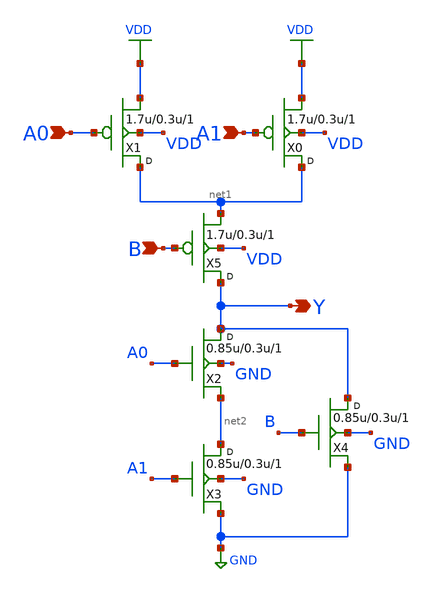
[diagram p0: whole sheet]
** sch_path: openfasoc/common/platforms/gf180mcuosu9Taoi211/gf180mcu_osu_sc_aoi21_1.sch
**.subckt gf180mcu_osu_sc_aoi21_1 A0 A1 Y B
*.ipin A0
*.ipin A1
*.opin Y
*.ipin B
X1 net1 A0 VDD VDD pmos_3p3 w=1.7u l=0.3u m=1
X0 net1 A1 VDD VDD pmos_3p3 w=1.7u l=0.3u m=1
X2 Y A0 net2 GND nmos_3p3 w=0.85u l=0.3u m=1
X3 net2 A1 GND GND nmos_3p3 w=0.85u l=0.3u m=1
X4 Y B GND GND nmos_3p3 w=0.85u l=0.3u m=1
X5 Y B net1 VDD pmos_3p3 w=1.7u l=0.3u m=1
**.ends
.GLOBAL VDD
.GLOBAL GND
.end
